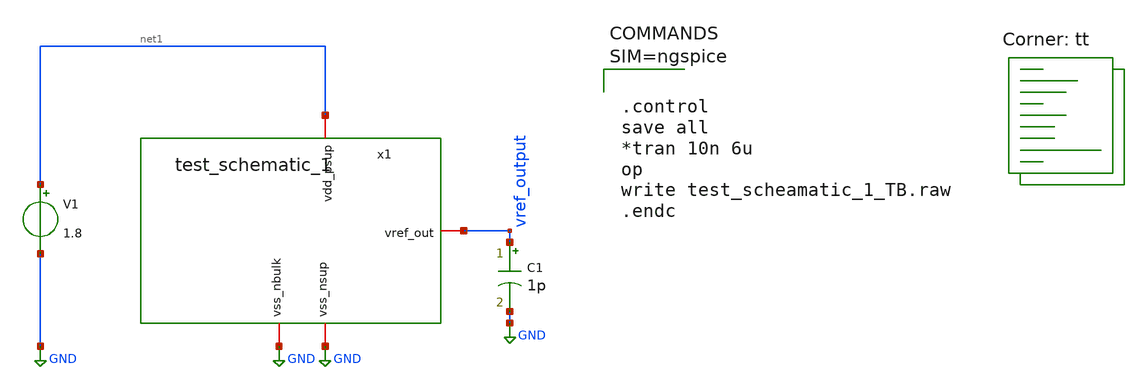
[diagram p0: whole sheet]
** sch_path: xschem/test_schematic_1_TB.sch
**.subckt test_schematic_1_TB
x1 net1 vref_output GND GND test_schematic_1
V1 net1 GND 1.8
C1 vref_output GND 1p m=1
**** begin user architecture code



.control
save all
*tran 10n 6u
op
write test_scheamatic_1_TB.raw
.endc



.lib $::SKYWATER_MODELS/sky130.lib.spice tt
**** end user architecture code
**.ends

* expanding   symbol:  test_schematic_1.sym # of pins=4
** sym_path: xschem/test_schematic_1.sym
** sch_path: xschem/test_schematic_1.sch
.subckt test_schematic_1 vdd_psup vref_out vss_nbulk vss_nsup
*.iopin vdd_psup
*.iopin vss_nbulk
*.iopin vss_nsup
*.iopin vref_out
XM1 vref_out vref_out vss_nsup vss_nbulk sky130_fd_pr__nfet_01v8_lvt L=0.15 W=1 nf=1 ad='int((nf+1)/2) * W/nf * 0.29'
+ as='int((nf+2)/2) * W/nf * 0.29' pd='2*int((nf+1)/2) * (W/nf + 0.29)' ps='2*int((nf+2)/2) * (W/nf + 0.29)'
+ nrd='0.29 / W' nrs='0.29 / W' sa=0 sb=0 sd=0 mult=1 m=1
XM2 vdd_psup vss_nsup vref_out vss_nbulk sky130_fd_pr__nfet_03v3_nvt L=0.5 W=1 nf=1 ad='int((nf+1)/2) * W/nf * 0.29'
+ as='int((nf+2)/2) * W/nf * 0.29' pd='2*int((nf+1)/2) * (W/nf + 0.29)' ps='2*int((nf+2)/2) * (W/nf + 0.29)'
+ nrd='0.29 / W' nrs='0.29 / W' sa=0 sb=0 sd=0 mult=1 m=1
.ends

.GLOBAL GND
.end
